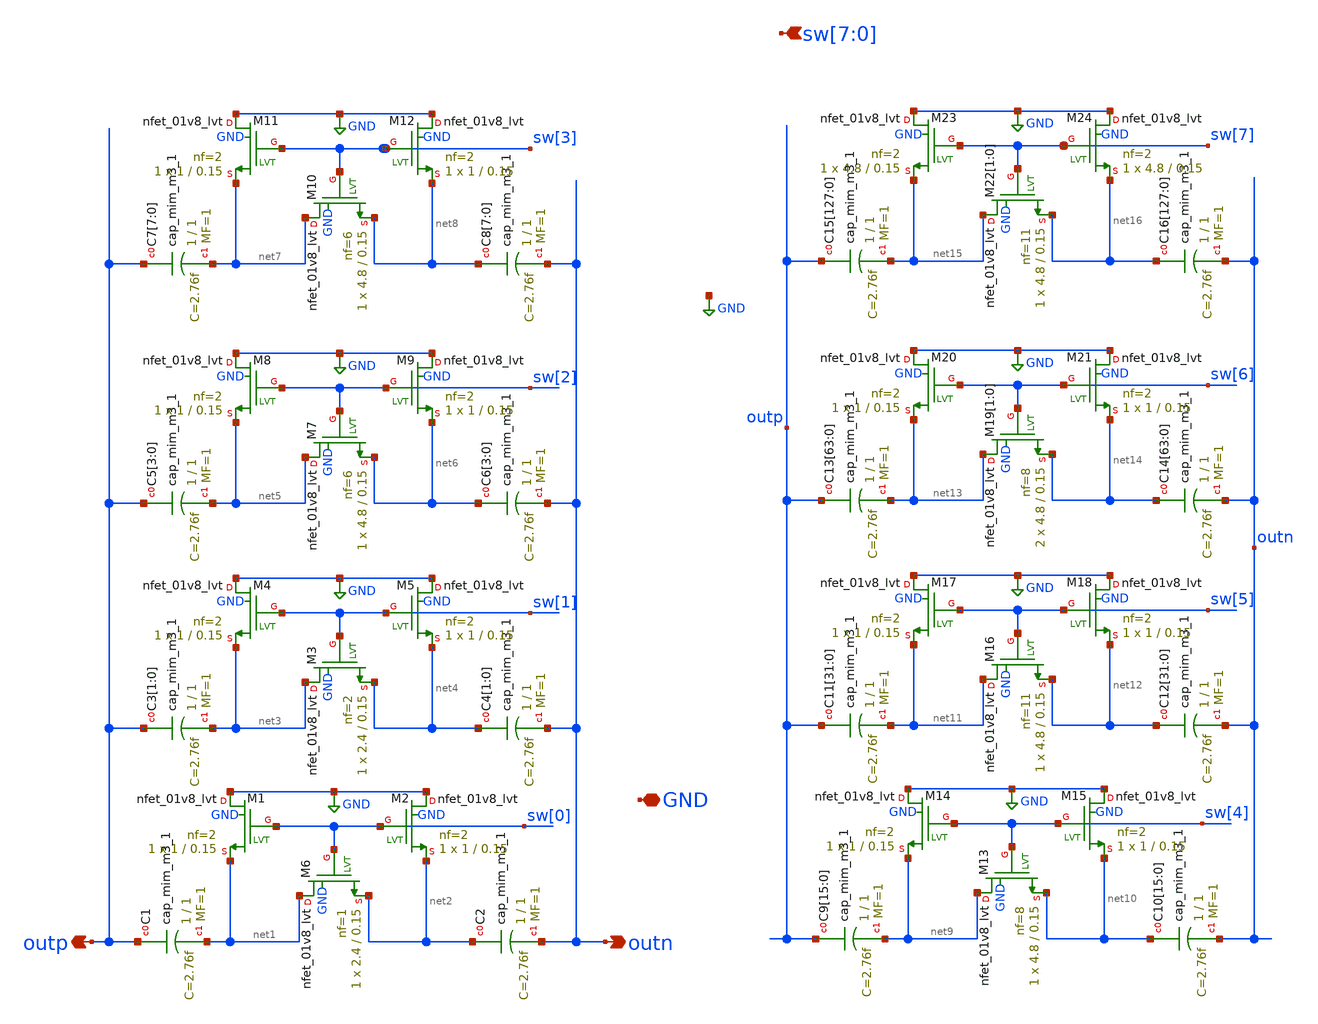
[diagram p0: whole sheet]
** sch_path: openfasoc/generators/lc-dco/xschem_rundir/swcap_3M2C.sch
**.subckt swcap_3M2C outn outp sw[7],sw[6],sw[5],sw[4],sw[3],sw[2],sw[1],sw[0] GND
*.opin outn
*.opin outp
*.ipin sw[7],sw[6],sw[5],sw[4],sw[3],sw[2],sw[1],sw[0]
*.iopin GND
XC2 net2 outn sky130_fd_pr__cap_mim_m3_1 W=1 L=1 MF=1 m=1
XM6 net1 sw[0] net2 GND sky130_fd_pr__nfet_01v8_lvt L=0.15 W=2.4 nf=1 ad='int((nf+1)/2) * W/nf * 0.29'
+ as='int((nf+2)/2) * W/nf * 0.29' pd='2*int((nf+1)/2) * (W/nf + 0.29)' ps='2*int((nf+2)/2) * (W/nf + 0.29)'
+ nrd='0.29 / W' nrs='0.29 / W' sa=0 sb=0 sd=0 mult=1 m=1
XM1 GND sw[0] net1 GND sky130_fd_pr__nfet_01v8_lvt L=0.15 W=1 nf=2 ad='int((nf+1)/2) * W/nf * 0.29' as='int((nf+2)/2) * W/nf * 0.29'
+ pd='2*int((nf+1)/2) * (W/nf + 0.29)' ps='2*int((nf+2)/2) * (W/nf + 0.29)' nrd='0.29 / W' nrs='0.29 / W'
+ sa=0 sb=0 sd=0 mult=1 m=1
XM2 GND sw[0] net2 GND sky130_fd_pr__nfet_01v8_lvt L=0.15 W=1 nf=2 ad='int((nf+1)/2) * W/nf * 0.29' as='int((nf+2)/2) * W/nf * 0.29'
+ pd='2*int((nf+1)/2) * (W/nf + 0.29)' ps='2*int((nf+2)/2) * (W/nf + 0.29)' nrd='0.29 / W' nrs='0.29 / W'
+ sa=0 sb=0 sd=0 mult=1 m=1
XC1 outp net1 sky130_fd_pr__cap_mim_m3_1 W=1 L=1 MF=1 m=1
XC4[1] net4 outn sky130_fd_pr__cap_mim_m3_1 W=1 L=1 MF=1 m=1
XC4[0] net4 outn sky130_fd_pr__cap_mim_m3_1 W=1 L=1 MF=1 m=1
XM3 net3 sw[1] net4 GND sky130_fd_pr__nfet_01v8_lvt L=0.15 W=2.4 nf=2 ad='int((nf+1)/2) * W/nf * 0.29'
+ as='int((nf+2)/2) * W/nf * 0.29' pd='2*int((nf+1)/2) * (W/nf + 0.29)' ps='2*int((nf+2)/2) * (W/nf + 0.29)'
+ nrd='0.29 / W' nrs='0.29 / W' sa=0 sb=0 sd=0 mult=1 m=1
XM4 GND sw[1] net3 GND sky130_fd_pr__nfet_01v8_lvt L=0.15 W=1 nf=2 ad='int((nf+1)/2) * W/nf * 0.29' as='int((nf+2)/2) * W/nf * 0.29'
+ pd='2*int((nf+1)/2) * (W/nf + 0.29)' ps='2*int((nf+2)/2) * (W/nf + 0.29)' nrd='0.29 / W' nrs='0.29 / W'
+ sa=0 sb=0 sd=0 mult=1 m=1
XM5 GND sw[1] net4 GND sky130_fd_pr__nfet_01v8_lvt L=0.15 W=1 nf=2 ad='int((nf+1)/2) * W/nf * 0.29' as='int((nf+2)/2) * W/nf * 0.29'
+ pd='2*int((nf+1)/2) * (W/nf + 0.29)' ps='2*int((nf+2)/2) * (W/nf + 0.29)' nrd='0.29 / W' nrs='0.29 / W'
+ sa=0 sb=0 sd=0 mult=1 m=1
XC3[1] outp net3 sky130_fd_pr__cap_mim_m3_1 W=1 L=1 MF=1 m=1
XC3[0] outp net3 sky130_fd_pr__cap_mim_m3_1 W=1 L=1 MF=1 m=1
XC6[3] net6 outn sky130_fd_pr__cap_mim_m3_1 W=1 L=1 MF=1 m=1
XC6[2] net6 outn sky130_fd_pr__cap_mim_m3_1 W=1 L=1 MF=1 m=1
XC6[1] net6 outn sky130_fd_pr__cap_mim_m3_1 W=1 L=1 MF=1 m=1
XC6[0] net6 outn sky130_fd_pr__cap_mim_m3_1 W=1 L=1 MF=1 m=1
XM7 net5 sw[2] net6 GND sky130_fd_pr__nfet_01v8_lvt L=0.15 W=4.8 nf=6 ad='int((nf+1)/2) * W/nf * 0.29'
+ as='int((nf+2)/2) * W/nf * 0.29' pd='2*int((nf+1)/2) * (W/nf + 0.29)' ps='2*int((nf+2)/2) * (W/nf + 0.29)'
+ nrd='0.29 / W' nrs='0.29 / W' sa=0 sb=0 sd=0 mult=1 m=1
XM8 GND sw[2] net5 GND sky130_fd_pr__nfet_01v8_lvt L=0.15 W=1 nf=2 ad='int((nf+1)/2) * W/nf * 0.29' as='int((nf+2)/2) * W/nf * 0.29'
+ pd='2*int((nf+1)/2) * (W/nf + 0.29)' ps='2*int((nf+2)/2) * (W/nf + 0.29)' nrd='0.29 / W' nrs='0.29 / W'
+ sa=0 sb=0 sd=0 mult=1 m=1
XM9 GND sw[2] net6 GND sky130_fd_pr__nfet_01v8_lvt L=0.15 W=1 nf=2 ad='int((nf+1)/2) * W/nf * 0.29' as='int((nf+2)/2) * W/nf * 0.29'
+ pd='2*int((nf+1)/2) * (W/nf + 0.29)' ps='2*int((nf+2)/2) * (W/nf + 0.29)' nrd='0.29 / W' nrs='0.29 / W'
+ sa=0 sb=0 sd=0 mult=1 m=1
XC5[3] outp net5 sky130_fd_pr__cap_mim_m3_1 W=1 L=1 MF=1 m=1
XC5[2] outp net5 sky130_fd_pr__cap_mim_m3_1 W=1 L=1 MF=1 m=1
XC5[1] outp net5 sky130_fd_pr__cap_mim_m3_1 W=1 L=1 MF=1 m=1
XC5[0] outp net5 sky130_fd_pr__cap_mim_m3_1 W=1 L=1 MF=1 m=1
XC8[7] net8 outn sky130_fd_pr__cap_mim_m3_1 W=1 L=1 MF=1 m=1
XC8[6] net8 outn sky130_fd_pr__cap_mim_m3_1 W=1 L=1 MF=1 m=1
XC8[5] net8 outn sky130_fd_pr__cap_mim_m3_1 W=1 L=1 MF=1 m=1
XC8[4] net8 outn sky130_fd_pr__cap_mim_m3_1 W=1 L=1 MF=1 m=1
XC8[3] net8 outn sky130_fd_pr__cap_mim_m3_1 W=1 L=1 MF=1 m=1
XC8[2] net8 outn sky130_fd_pr__cap_mim_m3_1 W=1 L=1 MF=1 m=1
XC8[1] net8 outn sky130_fd_pr__cap_mim_m3_1 W=1 L=1 MF=1 m=1
XC8[0] net8 outn sky130_fd_pr__cap_mim_m3_1 W=1 L=1 MF=1 m=1
XM10 net7 sw[3] net8 GND sky130_fd_pr__nfet_01v8_lvt L=0.15 W=4.8 nf=6 ad='int((nf+1)/2) * W/nf * 0.29'
+ as='int((nf+2)/2) * W/nf * 0.29' pd='2*int((nf+1)/2) * (W/nf + 0.29)' ps='2*int((nf+2)/2) * (W/nf + 0.29)'
+ nrd='0.29 / W' nrs='0.29 / W' sa=0 sb=0 sd=0 mult=1 m=1
XM11 GND sw[3] net7 GND sky130_fd_pr__nfet_01v8_lvt L=0.15 W=1 nf=2 ad='int((nf+1)/2) * W/nf * 0.29'
+ as='int((nf+2)/2) * W/nf * 0.29' pd='2*int((nf+1)/2) * (W/nf + 0.29)' ps='2*int((nf+2)/2) * (W/nf + 0.29)'
+ nrd='0.29 / W' nrs='0.29 / W' sa=0 sb=0 sd=0 mult=1 m=1
XM12 GND sw[3] net8 GND sky130_fd_pr__nfet_01v8_lvt L=0.15 W=1 nf=2 ad='int((nf+1)/2) * W/nf * 0.29'
+ as='int((nf+2)/2) * W/nf * 0.29' pd='2*int((nf+1)/2) * (W/nf + 0.29)' ps='2*int((nf+2)/2) * (W/nf + 0.29)'
+ nrd='0.29 / W' nrs='0.29 / W' sa=0 sb=0 sd=0 mult=1 m=1
XC7[7] outp net7 sky130_fd_pr__cap_mim_m3_1 W=1 L=1 MF=1 m=1
XC7[6] outp net7 sky130_fd_pr__cap_mim_m3_1 W=1 L=1 MF=1 m=1
XC7[5] outp net7 sky130_fd_pr__cap_mim_m3_1 W=1 L=1 MF=1 m=1
XC7[4] outp net7 sky130_fd_pr__cap_mim_m3_1 W=1 L=1 MF=1 m=1
XC7[3] outp net7 sky130_fd_pr__cap_mim_m3_1 W=1 L=1 MF=1 m=1
XC7[2] outp net7 sky130_fd_pr__cap_mim_m3_1 W=1 L=1 MF=1 m=1
XC7[1] outp net7 sky130_fd_pr__cap_mim_m3_1 W=1 L=1 MF=1 m=1
XC7[0] outp net7 sky130_fd_pr__cap_mim_m3_1 W=1 L=1 MF=1 m=1
XC10[15] net10 outn sky130_fd_pr__cap_mim_m3_1 W=1 L=1 MF=1 m=1
XC10[14] net10 outn sky130_fd_pr__cap_mim_m3_1 W=1 L=1 MF=1 m=1
XC10[13] net10 outn sky130_fd_pr__cap_mim_m3_1 W=1 L=1 MF=1 m=1
XC10[12] net10 outn sky130_fd_pr__cap_mim_m3_1 W=1 L=1 MF=1 m=1
XC10[11] net10 outn sky130_fd_pr__cap_mim_m3_1 W=1 L=1 MF=1 m=1
XC10[10] net10 outn sky130_fd_pr__cap_mim_m3_1 W=1 L=1 MF=1 m=1
XC10[9] net10 outn sky130_fd_pr__cap_mim_m3_1 W=1 L=1 MF=1 m=1
XC10[8] net10 outn sky130_fd_pr__cap_mim_m3_1 W=1 L=1 MF=1 m=1
XC10[7] net10 outn sky130_fd_pr__cap_mim_m3_1 W=1 L=1 MF=1 m=1
XC10[6] net10 outn sky130_fd_pr__cap_mim_m3_1 W=1 L=1 MF=1 m=1
XC10[5] net10 outn sky130_fd_pr__cap_mim_m3_1 W=1 L=1 MF=1 m=1
XC10[4] net10 outn sky130_fd_pr__cap_mim_m3_1 W=1 L=1 MF=1 m=1
XC10[3] net10 outn sky130_fd_pr__cap_mim_m3_1 W=1 L=1 MF=1 m=1
XC10[2] net10 outn sky130_fd_pr__cap_mim_m3_1 W=1 L=1 MF=1 m=1
XC10[1] net10 outn sky130_fd_pr__cap_mim_m3_1 W=1 L=1 MF=1 m=1
XC10[0] net10 outn sky130_fd_pr__cap_mim_m3_1 W=1 L=1 MF=1 m=1
XM13 net9 sw[4] net10 GND sky130_fd_pr__nfet_01v8_lvt L=0.15 W=4.8 nf=8 ad='int((nf+1)/2) * W/nf * 0.29'
+ as='int((nf+2)/2) * W/nf * 0.29' pd='2*int((nf+1)/2) * (W/nf + 0.29)' ps='2*int((nf+2)/2) * (W/nf + 0.29)'
+ nrd='0.29 / W' nrs='0.29 / W' sa=0 sb=0 sd=0 mult=1 m=1
XM14 GND sw[4] net9 GND sky130_fd_pr__nfet_01v8_lvt L=0.15 W=1 nf=2 ad='int((nf+1)/2) * W/nf * 0.29'
+ as='int((nf+2)/2) * W/nf * 0.29' pd='2*int((nf+1)/2) * (W/nf + 0.29)' ps='2*int((nf+2)/2) * (W/nf + 0.29)'
+ nrd='0.29 / W' nrs='0.29 / W' sa=0 sb=0 sd=0 mult=1 m=1
XM15 GND sw[4] net10 GND sky130_fd_pr__nfet_01v8_lvt L=0.15 W=1 nf=2 ad='int((nf+1)/2) * W/nf * 0.29'
+ as='int((nf+2)/2) * W/nf * 0.29' pd='2*int((nf+1)/2) * (W/nf + 0.29)' ps='2*int((nf+2)/2) * (W/nf + 0.29)'
+ nrd='0.29 / W' nrs='0.29 / W' sa=0 sb=0 sd=0 mult=1 m=1
XC9[15] outp net9 sky130_fd_pr__cap_mim_m3_1 W=1 L=1 MF=1 m=1
XC9[14] outp net9 sky130_fd_pr__cap_mim_m3_1 W=1 L=1 MF=1 m=1
XC9[13] outp net9 sky130_fd_pr__cap_mim_m3_1 W=1 L=1 MF=1 m=1
XC9[12] outp net9 sky130_fd_pr__cap_mim_m3_1 W=1 L=1 MF=1 m=1
XC9[11] outp net9 sky130_fd_pr__cap_mim_m3_1 W=1 L=1 MF=1 m=1
XC9[10] outp net9 sky130_fd_pr__cap_mim_m3_1 W=1 L=1 MF=1 m=1
XC9[9] outp net9 sky130_fd_pr__cap_mim_m3_1 W=1 L=1 MF=1 m=1
XC9[8] outp net9 sky130_fd_pr__cap_mim_m3_1 W=1 L=1 MF=1 m=1
XC9[7] outp net9 sky130_fd_pr__cap_mim_m3_1 W=1 L=1 MF=1 m=1
XC9[6] outp net9 sky130_fd_pr__cap_mim_m3_1 W=1 L=1 MF=1 m=1
XC9[5] outp net9 sky130_fd_pr__cap_mim_m3_1 W=1 L=1 MF=1 m=1
XC9[4] outp net9 sky130_fd_pr__cap_mim_m3_1 W=1 L=1 MF=1 m=1
XC9[3] outp net9 sky130_fd_pr__cap_mim_m3_1 W=1 L=1 MF=1 m=1
XC9[2] outp net9 sky130_fd_pr__cap_mim_m3_1 W=1 L=1 MF=1 m=1
XC9[1] outp net9 sky130_fd_pr__cap_mim_m3_1 W=1 L=1 MF=1 m=1
XC9[0] outp net9 sky130_fd_pr__cap_mim_m3_1 W=1 L=1 MF=1 m=1
XC12[31] net12 outn sky130_fd_pr__cap_mim_m3_1 W=1 L=1 MF=1 m=1
XC12[30] net12 outn sky130_fd_pr__cap_mim_m3_1 W=1 L=1 MF=1 m=1
XC12[29] net12 outn sky130_fd_pr__cap_mim_m3_1 W=1 L=1 MF=1 m=1
XC12[28] net12 outn sky130_fd_pr__cap_mim_m3_1 W=1 L=1 MF=1 m=1
XC12[27] net12 outn sky130_fd_pr__cap_mim_m3_1 W=1 L=1 MF=1 m=1
XC12[26] net12 outn sky130_fd_pr__cap_mim_m3_1 W=1 L=1 MF=1 m=1
XC12[25] net12 outn sky130_fd_pr__cap_mim_m3_1 W=1 L=1 MF=1 m=1
XC12[24] net12 outn sky130_fd_pr__cap_mim_m3_1 W=1 L=1 MF=1 m=1
XC12[23] net12 outn sky130_fd_pr__cap_mim_m3_1 W=1 L=1 MF=1 m=1
XC12[22] net12 outn sky130_fd_pr__cap_mim_m3_1 W=1 L=1 MF=1 m=1
XC12[21] net12 outn sky130_fd_pr__cap_mim_m3_1 W=1 L=1 MF=1 m=1
XC12[20] net12 outn sky130_fd_pr__cap_mim_m3_1 W=1 L=1 MF=1 m=1
XC12[19] net12 outn sky130_fd_pr__cap_mim_m3_1 W=1 L=1 MF=1 m=1
XC12[18] net12 outn sky130_fd_pr__cap_mim_m3_1 W=1 L=1 MF=1 m=1
XC12[17] net12 outn sky130_fd_pr__cap_mim_m3_1 W=1 L=1 MF=1 m=1
XC12[16] net12 outn sky130_fd_pr__cap_mim_m3_1 W=1 L=1 MF=1 m=1
XC12[15] net12 outn sky130_fd_pr__cap_mim_m3_1 W=1 L=1 MF=1 m=1
XC12[14] net12 outn sky130_fd_pr__cap_mim_m3_1 W=1 L=1 MF=1 m=1
XC12[13] net12 outn sky130_fd_pr__cap_mim_m3_1 W=1 L=1 MF=1 m=1
XC12[12] net12 outn sky130_fd_pr__cap_mim_m3_1 W=1 L=1 MF=1 m=1
XC12[11] net12 outn sky130_fd_pr__cap_mim_m3_1 W=1 L=1 MF=1 m=1
XC12[10] net12 outn sky130_fd_pr__cap_mim_m3_1 W=1 L=1 MF=1 m=1
XC12[9] net12 outn sky130_fd_pr__cap_mim_m3_1 W=1 L=1 MF=1 m=1
XC12[8] net12 outn sky130_fd_pr__cap_mim_m3_1 W=1 L=1 MF=1 m=1
XC12[7] net12 outn sky130_fd_pr__cap_mim_m3_1 W=1 L=1 MF=1 m=1
XC12[6] net12 outn sky130_fd_pr__cap_mim_m3_1 W=1 L=1 MF=1 m=1
XC12[5] net12 outn sky130_fd_pr__cap_mim_m3_1 W=1 L=1 MF=1 m=1
XC12[4] net12 outn sky130_fd_pr__cap_mim_m3_1 W=1 L=1 MF=1 m=1
XC12[3] net12 outn sky130_fd_pr__cap_mim_m3_1 W=1 L=1 MF=1 m=1
XC12[2] net12 outn sky130_fd_pr__cap_mim_m3_1 W=1 L=1 MF=1 m=1
XC12[1] net12 outn sky130_fd_pr__cap_mim_m3_1 W=1 L=1 MF=1 m=1
XC12[0] net12 outn sky130_fd_pr__cap_mim_m3_1 W=1 L=1 MF=1 m=1
XM16 net11 sw[5] net12 GND sky130_fd_pr__nfet_01v8_lvt L=0.15 W=4.8 nf=11 ad='int((nf+1)/2) * W/nf * 0.29'
+ as='int((nf+2)/2) * W/nf * 0.29' pd='2*int((nf+1)/2) * (W/nf + 0.29)' ps='2*int((nf+2)/2) * (W/nf + 0.29)'
+ nrd='0.29 / W' nrs='0.29 / W' sa=0 sb=0 sd=0 mult=1 m=1
XM17 GND sw[5] net11 GND sky130_fd_pr__nfet_01v8_lvt L=0.15 W=1 nf=2 ad='int((nf+1)/2) * W/nf * 0.29'
+ as='int((nf+2)/2) * W/nf * 0.29' pd='2*int((nf+1)/2) * (W/nf + 0.29)' ps='2*int((nf+2)/2) * (W/nf + 0.29)'
+ nrd='0.29 / W' nrs='0.29 / W' sa=0 sb=0 sd=0 mult=1 m=1
XM18 GND sw[5] net12 GND sky130_fd_pr__nfet_01v8_lvt L=0.15 W=1 nf=2 ad='int((nf+1)/2) * W/nf * 0.29'
+ as='int((nf+2)/2) * W/nf * 0.29' pd='2*int((nf+1)/2) * (W/nf + 0.29)' ps='2*int((nf+2)/2) * (W/nf + 0.29)'
+ nrd='0.29 / W' nrs='0.29 / W' sa=0 sb=0 sd=0 mult=1 m=1
XC11[31] outp net11 sky130_fd_pr__cap_mim_m3_1 W=1 L=1 MF=1 m=1
XC11[30] outp net11 sky130_fd_pr__cap_mim_m3_1 W=1 L=1 MF=1 m=1
XC11[29] outp net11 sky130_fd_pr__cap_mim_m3_1 W=1 L=1 MF=1 m=1
XC11[28] outp net11 sky130_fd_pr__cap_mim_m3_1 W=1 L=1 MF=1 m=1
XC11[27] outp net11 sky130_fd_pr__cap_mim_m3_1 W=1 L=1 MF=1 m=1
XC11[26] outp net11 sky130_fd_pr__cap_mim_m3_1 W=1 L=1 MF=1 m=1
XC11[25] outp net11 sky130_fd_pr__cap_mim_m3_1 W=1 L=1 MF=1 m=1
XC11[24] outp net11 sky130_fd_pr__cap_mim_m3_1 W=1 L=1 MF=1 m=1
XC11[23] outp net11 sky130_fd_pr__cap_mim_m3_1 W=1 L=1 MF=1 m=1
XC11[22] outp net11 sky130_fd_pr__cap_mim_m3_1 W=1 L=1 MF=1 m=1
XC11[21] outp net11 sky130_fd_pr__cap_mim_m3_1 W=1 L=1 MF=1 m=1
XC11[20] outp net11 sky130_fd_pr__cap_mim_m3_1 W=1 L=1 MF=1 m=1
XC11[19] outp net11 sky130_fd_pr__cap_mim_m3_1 W=1 L=1 MF=1 m=1
XC11[18] outp net11 sky130_fd_pr__cap_mim_m3_1 W=1 L=1 MF=1 m=1
XC11[17] outp net11 sky130_fd_pr__cap_mim_m3_1 W=1 L=1 MF=1 m=1
XC11[16] outp net11 sky130_fd_pr__cap_mim_m3_1 W=1 L=1 MF=1 m=1
XC11[15] outp net11 sky130_fd_pr__cap_mim_m3_1 W=1 L=1 MF=1 m=1
XC11[14] outp net11 sky130_fd_pr__cap_mim_m3_1 W=1 L=1 MF=1 m=1
XC11[13] outp net11 sky130_fd_pr__cap_mim_m3_1 W=1 L=1 MF=1 m=1
XC11[12] outp net11 sky130_fd_pr__cap_mim_m3_1 W=1 L=1 MF=1 m=1
XC11[11] outp net11 sky130_fd_pr__cap_mim_m3_1 W=1 L=1 MF=1 m=1
XC11[10] outp net11 sky130_fd_pr__cap_mim_m3_1 W=1 L=1 MF=1 m=1
XC11[9] outp net11 sky130_fd_pr__cap_mim_m3_1 W=1 L=1 MF=1 m=1
XC11[8] outp net11 sky130_fd_pr__cap_mim_m3_1 W=1 L=1 MF=1 m=1
XC11[7] outp net11 sky130_fd_pr__cap_mim_m3_1 W=1 L=1 MF=1 m=1
XC11[6] outp net11 sky130_fd_pr__cap_mim_m3_1 W=1 L=1 MF=1 m=1
XC11[5] outp net11 sky130_fd_pr__cap_mim_m3_1 W=1 L=1 MF=1 m=1
XC11[4] outp net11 sky130_fd_pr__cap_mim_m3_1 W=1 L=1 MF=1 m=1
XC11[3] outp net11 sky130_fd_pr__cap_mim_m3_1 W=1 L=1 MF=1 m=1
XC11[2] outp net11 sky130_fd_pr__cap_mim_m3_1 W=1 L=1 MF=1 m=1
XC11[1] outp net11 sky130_fd_pr__cap_mim_m3_1 W=1 L=1 MF=1 m=1
XC11[0] outp net11 sky130_fd_pr__cap_mim_m3_1 W=1 L=1 MF=1 m=1
XC14[63] net14 outn sky130_fd_pr__cap_mim_m3_1 W=1 L=1 MF=1 m=1
XC14[62] net14 outn sky130_fd_pr__cap_mim_m3_1 W=1 L=1 MF=1 m=1
XC14[61] net14 outn sky130_fd_pr__cap_mim_m3_1 W=1 L=1 MF=1 m=1
XC14[60] net14 outn sky130_fd_pr__cap_mim_m3_1 W=1 L=1 MF=1 m=1
XC14[59] net14 outn sky130_fd_pr__cap_mim_m3_1 W=1 L=1 MF=1 m=1
XC14[58] net14 outn sky130_fd_pr__cap_mim_m3_1 W=1 L=1 MF=1 m=1
XC14[57] net14 outn sky130_fd_pr__cap_mim_m3_1 W=1 L=1 MF=1 m=1
XC14[56] net14 outn sky130_fd_pr__cap_mim_m3_1 W=1 L=1 MF=1 m=1
XC14[55] net14 outn sky130_fd_pr__cap_mim_m3_1 W=1 L=1 MF=1 m=1
XC14[54] net14 outn sky130_fd_pr__cap_mim_m3_1 W=1 L=1 MF=1 m=1
XC14[53] net14 outn sky130_fd_pr__cap_mim_m3_1 W=1 L=1 MF=1 m=1
XC14[52] net14 outn sky130_fd_pr__cap_mim_m3_1 W=1 L=1 MF=1 m=1
XC14[51] net14 outn sky130_fd_pr__cap_mim_m3_1 W=1 L=1 MF=1 m=1
XC14[50] net14 outn sky130_fd_pr__cap_mim_m3_1 W=1 L=1 MF=1 m=1
XC14[49] net14 outn sky130_fd_pr__cap_mim_m3_1 W=1 L=1 MF=1 m=1
XC14[48] net14 outn sky130_fd_pr__cap_mim_m3_1 W=1 L=1 MF=1 m=1
XC14[47] net14 outn sky130_fd_pr__cap_mim_m3_1 W=1 L=1 MF=1 m=1
XC14[46] net14 outn sky130_fd_pr__cap_mim_m3_1 W=1 L=1 MF=1 m=1
XC14[45] net14 outn sky130_fd_pr__cap_mim_m3_1 W=1 L=1 MF=1 m=1
XC14[44] net14 outn sky130_fd_pr__cap_mim_m3_1 W=1 L=1 MF=1 m=1
XC14[43] net14 outn sky130_fd_pr__cap_mim_m3_1 W=1 L=1 MF=1 m=1
XC14[42] net14 outn sky130_fd_pr__cap_mim_m3_1 W=1 L=1 MF=1 m=1
XC14[41] net14 outn sky130_fd_pr__cap_mim_m3_1 W=1 L=1 MF=1 m=1
XC14[40] net14 outn sky130_fd_pr__cap_mim_m3_1 W=1 L=1 MF=1 m=1
XC14[39] net14 outn sky130_fd_pr__cap_mim_m3_1 W=1 L=1 MF=1 m=1
XC14[38] net14 outn sky130_fd_pr__cap_mim_m3_1 W=1 L=1 MF=1 m=1
XC14[37] net14 outn sky130_fd_pr__cap_mim_m3_1 W=1 L=1 MF=1 m=1
XC14[36] net14 outn sky130_fd_pr__cap_mim_m3_1 W=1 L=1 MF=1 m=1
XC14[35] net14 outn sky130_fd_pr__cap_mim_m3_1 W=1 L=1 MF=1 m=1
XC14[34] net14 outn sky130_fd_pr__cap_mim_m3_1 W=1 L=1 MF=1 m=1
XC14[33] net14 outn sky130_fd_pr__cap_mim_m3_1 W=1 L=1 MF=1 m=1
XC14[32] net14 outn sky130_fd_pr__cap_mim_m3_1 W=1 L=1 MF=1 m=1
XC14[31] net14 outn sky130_fd_pr__cap_mim_m3_1 W=1 L=1 MF=1 m=1
XC14[30] net14 outn sky130_fd_pr__cap_mim_m3_1 W=1 L=1 MF=1 m=1
XC14[29] net14 outn sky130_fd_pr__cap_mim_m3_1 W=1 L=1 MF=1 m=1
XC14[28] net14 outn sky130_fd_pr__cap_mim_m3_1 W=1 L=1 MF=1 m=1
XC14[27] net14 outn sky130_fd_pr__cap_mim_m3_1 W=1 L=1 MF=1 m=1
XC14[26] net14 outn sky130_fd_pr__cap_mim_m3_1 W=1 L=1 MF=1 m=1
XC14[25] net14 outn sky130_fd_pr__cap_mim_m3_1 W=1 L=1 MF=1 m=1
XC14[24] net14 outn sky130_fd_pr__cap_mim_m3_1 W=1 L=1 MF=1 m=1
XC14[23] net14 outn sky130_fd_pr__cap_mim_m3_1 W=1 L=1 MF=1 m=1
XC14[22] net14 outn sky130_fd_pr__cap_mim_m3_1 W=1 L=1 MF=1 m=1
XC14[21] net14 outn sky130_fd_pr__cap_mim_m3_1 W=1 L=1 MF=1 m=1
XC14[20] net14 outn sky130_fd_pr__cap_mim_m3_1 W=1 L=1 MF=1 m=1
XC14[19] net14 outn sky130_fd_pr__cap_mim_m3_1 W=1 L=1 MF=1 m=1
XC14[18] net14 outn sky130_fd_pr__cap_mim_m3_1 W=1 L=1 MF=1 m=1
XC14[17] net14 outn sky130_fd_pr__cap_mim_m3_1 W=1 L=1 MF=1 m=1
XC14[16] net14 outn sky130_fd_pr__cap_mim_m3_1 W=1 L=1 MF=1 m=1
XC14[15] net14 outn sky130_fd_pr__cap_mim_m3_1 W=1 L=1 MF=1 m=1
XC14[14] net14 outn sky130_fd_pr__cap_mim_m3_1 W=1 L=1 MF=1 m=1
XC14[13] net14 outn sky130_fd_pr__cap_mim_m3_1 W=1 L=1 MF=1 m=1
XC14[12] net14 outn sky130_fd_pr__cap_mim_m3_1 W=1 L=1 MF=1 m=1
XC14[11] net14 outn sky130_fd_pr__cap_mim_m3_1 W=1 L=1 MF=1 m=1
XC14[10] net14 outn sky130_fd_pr__cap_mim_m3_1 W=1 L=1 MF=1 m=1
XC14[9] net14 outn sky130_fd_pr__cap_mim_m3_1 W=1 L=1 MF=1 m=1
XC14[8] net14 outn sky130_fd_pr__cap_mim_m3_1 W=1 L=1 MF=1 m=1
XC14[7] net14 outn sky130_fd_pr__cap_mim_m3_1 W=1 L=1 MF=1 m=1
XC14[6] net14 outn sky130_fd_pr__cap_mim_m3_1 W=1 L=1 MF=1 m=1
XC14[5] net14 outn sky130_fd_pr__cap_mim_m3_1 W=1 L=1 MF=1 m=1
XC14[4] net14 outn sky130_fd_pr__cap_mim_m3_1 W=1 L=1 MF=1 m=1
XC14[3] net14 outn sky130_fd_pr__cap_mim_m3_1 W=1 L=1 MF=1 m=1
XC14[2] net14 outn sky130_fd_pr__cap_mim_m3_1 W=1 L=1 MF=1 m=1
XC14[1] net14 outn sky130_fd_pr__cap_mim_m3_1 W=1 L=1 MF=1 m=1
XC14[0] net14 outn sky130_fd_pr__cap_mim_m3_1 W=1 L=1 MF=1 m=1
XM19[1] net13 sw[6] net14 GND sky130_fd_pr__nfet_01v8_lvt L=0.15 W=4.8 nf=8 ad='int((nf+1)/2) * W/nf * 0.29'
+ as='int((nf+2)/2) * W/nf * 0.29' pd='2*int((nf+1)/2) * (W/nf + 0.29)' ps='2*int((nf+2)/2) * (W/nf + 0.29)'
+ nrd='0.29 / W' nrs='0.29 / W' sa=0 sb=0 sd=0 mult=2 m=2
XM19[0] net13 sw[6] net14 GND sky130_fd_pr__nfet_01v8_lvt L=0.15 W=4.8 nf=8 ad='int((nf+1)/2) * W/nf * 0.29'
+ as='int((nf+2)/2) * W/nf * 0.29' pd='2*int((nf+1)/2) * (W/nf + 0.29)' ps='2*int((nf+2)/2) * (W/nf + 0.29)'
+ nrd='0.29 / W' nrs='0.29 / W' sa=0 sb=0 sd=0 mult=2 m=2
XM20 GND sw[6] net13 GND sky130_fd_pr__nfet_01v8_lvt L=0.15 W=1 nf=2 ad='int((nf+1)/2) * W/nf * 0.29'
+ as='int((nf+2)/2) * W/nf * 0.29' pd='2*int((nf+1)/2) * (W/nf + 0.29)' ps='2*int((nf+2)/2) * (W/nf + 0.29)'
+ nrd='0.29 / W' nrs='0.29 / W' sa=0 sb=0 sd=0 mult=1 m=1
XM21 GND sw[6] net14 GND sky130_fd_pr__nfet_01v8_lvt L=0.15 W=1 nf=2 ad='int((nf+1)/2) * W/nf * 0.29'
+ as='int((nf+2)/2) * W/nf * 0.29' pd='2*int((nf+1)/2) * (W/nf + 0.29)' ps='2*int((nf+2)/2) * (W/nf + 0.29)'
+ nrd='0.29 / W' nrs='0.29 / W' sa=0 sb=0 sd=0 mult=1 m=1
XC13[63] outp net13 sky130_fd_pr__cap_mim_m3_1 W=1 L=1 MF=1 m=1
XC13[62] outp net13 sky130_fd_pr__cap_mim_m3_1 W=1 L=1 MF=1 m=1
XC13[61] outp net13 sky130_fd_pr__cap_mim_m3_1 W=1 L=1 MF=1 m=1
XC13[60] outp net13 sky130_fd_pr__cap_mim_m3_1 W=1 L=1 MF=1 m=1
XC13[59] outp net13 sky130_fd_pr__cap_mim_m3_1 W=1 L=1 MF=1 m=1
XC13[58] outp net13 sky130_fd_pr__cap_mim_m3_1 W=1 L=1 MF=1 m=1
XC13[57] outp net13 sky130_fd_pr__cap_mim_m3_1 W=1 L=1 MF=1 m=1
XC13[56] outp net13 sky130_fd_pr__cap_mim_m3_1 W=1 L=1 MF=1 m=1
XC13[55] outp net13 sky130_fd_pr__cap_mim_m3_1 W=1 L=1 MF=1 m=1
XC13[54] outp net13 sky130_fd_pr__cap_mim_m3_1 W=1 L=1 MF=1 m=1
XC13[53] outp net13 sky130_fd_pr__cap_mim_m3_1 W=1 L=1 MF=1 m=1
XC13[52] outp net13 sky130_fd_pr__cap_mim_m3_1 W=1 L=1 MF=1 m=1
XC13[51] outp net13 sky130_fd_pr__cap_mim_m3_1 W=1 L=1 MF=1 m=1
XC13[50] outp net13 sky130_fd_pr__cap_mim_m3_1 W=1 L=1 MF=1 m=1
XC13[49] outp net13 sky130_fd_pr__cap_mim_m3_1 W=1 L=1 MF=1 m=1
XC13[48] outp net13 sky130_fd_pr__cap_mim_m3_1 W=1 L=1 MF=1 m=1
XC13[47] outp net13 sky130_fd_pr__cap_mim_m3_1 W=1 L=1 MF=1 m=1
XC13[46] outp net13 sky130_fd_pr__cap_mim_m3_1 W=1 L=1 MF=1 m=1
XC13[45] outp net13 sky130_fd_pr__cap_mim_m3_1 W=1 L=1 MF=1 m=1
XC13[44] outp net13 sky130_fd_pr__cap_mim_m3_1 W=1 L=1 MF=1 m=1
XC13[43] outp net13 sky130_fd_pr__cap_mim_m3_1 W=1 L=1 MF=1 m=1
XC13[42] outp net13 sky130_fd_pr__cap_mim_m3_1 W=1 L=1 MF=1 m=1
XC13[41] outp net13 sky130_fd_pr__cap_mim_m3_1 W=1 L=1 MF=1 m=1
XC13[40] outp net13 sky130_fd_pr__cap_mim_m3_1 W=1 L=1 MF=1 m=1
XC13[39] outp net13 sky130_fd_pr__cap_mim_m3_1 W=1 L=1 MF=1 m=1
XC13[38] outp net13 sky130_fd_pr__cap_mim_m3_1 W=1 L=1 MF=1 m=1
XC13[37] outp net13 sky130_fd_pr__cap_mim_m3_1 W=1 L=1 MF=1 m=1
XC13[36] outp net13 sky130_fd_pr__cap_mim_m3_1 W=1 L=1 MF=1 m=1
XC13[35] outp net13 sky130_fd_pr__cap_mim_m3_1 W=1 L=1 MF=1 m=1
XC13[34] outp net13 sky130_fd_pr__cap_mim_m3_1 W=1 L=1 MF=1 m=1
XC13[33] outp net13 sky130_fd_pr__cap_mim_m3_1 W=1 L=1 MF=1 m=1
XC13[32] outp net13 sky130_fd_pr__cap_mim_m3_1 W=1 L=1 MF=1 m=1
XC13[31] outp net13 sky130_fd_pr__cap_mim_m3_1 W=1 L=1 MF=1 m=1
XC13[30] outp net13 sky130_fd_pr__cap_mim_m3_1 W=1 L=1 MF=1 m=1
XC13[29] outp net13 sky130_fd_pr__cap_mim_m3_1 W=1 L=1 MF=1 m=1
XC13[28] outp net13 sky130_fd_pr__cap_mim_m3_1 W=1 L=1 MF=1 m=1
XC13[27] outp net13 sky130_fd_pr__cap_mim_m3_1 W=1 L=1 MF=1 m=1
XC13[26] outp net13 sky130_fd_pr__cap_mim_m3_1 W=1 L=1 MF=1 m=1
XC13[25] outp net13 sky130_fd_pr__cap_mim_m3_1 W=1 L=1 MF=1 m=1
XC13[24] outp net13 sky130_fd_pr__cap_mim_m3_1 W=1 L=1 MF=1 m=1
XC13[23] outp net13 sky130_fd_pr__cap_mim_m3_1 W=1 L=1 MF=1 m=1
XC13[22] outp net13 sky130_fd_pr__cap_mim_m3_1 W=1 L=1 MF=1 m=1
XC13[21] outp net13 sky130_fd_pr__cap_mim_m3_1 W=1 L=1 MF=1 m=1
XC13[20] outp net13 sky130_fd_pr__cap_mim_m3_1 W=1 L=1 MF=1 m=1
XC13[19] outp net13 sky130_fd_pr__cap_mim_m3_1 W=1 L=1 MF=1 m=1
XC13[18] outp net13 sky130_fd_pr__cap_mim_m3_1 W=1 L=1 MF=1 m=1
XC13[17] outp net13 sky130_fd_pr__cap_mim_m3_1 W=1 L=1 MF=1 m=1
XC13[16] outp net13 sky130_fd_pr__cap_mim_m3_1 W=1 L=1 MF=1 m=1
XC13[15] outp net13 sky130_fd_pr__cap_mim_m3_1 W=1 L=1 MF=1 m=1
XC13[14] outp net13 sky130_fd_pr__cap_mim_m3_1 W=1 L=1 MF=1 m=1
XC13[13] outp net13 sky130_fd_pr__cap_mim_m3_1 W=1 L=1 MF=1 m=1
XC13[12] outp net13 sky130_fd_pr__cap_mim_m3_1 W=1 L=1 MF=1 m=1
XC13[11] outp net13 sky130_fd_pr__cap_mim_m3_1 W=1 L=1 MF=1 m=1
XC13[10] outp net13 sky130_fd_pr__cap_mim_m3_1 W=1 L=1 MF=1 m=1
XC13[9] outp net13 sky130_fd_pr__cap_mim_m3_1 W=1 L=1 MF=1 m=1
XC13[8] outp net13 sky130_fd_pr__cap_mim_m3_1 W=1 L=1 MF=1 m=1
XC13[7] outp net13 sky130_fd_pr__cap_mim_m3_1 W=1 L=1 MF=1 m=1
XC13[6] outp net13 sky130_fd_pr__cap_mim_m3_1 W=1 L=1 MF=1 m=1
XC13[5] outp net13 sky130_fd_pr__cap_mim_m3_1 W=1 L=1 MF=1 m=1
XC13[4] outp net13 sky130_fd_pr__cap_mim_m3_1 W=1 L=1 MF=1 m=1
XC13[3] outp net13 sky130_fd_pr__cap_mim_m3_1 W=1 L=1 MF=1 m=1
XC13[2] outp net13 sky130_fd_pr__cap_mim_m3_1 W=1 L=1 MF=1 m=1
XC13[1] outp net13 sky130_fd_pr__cap_mim_m3_1 W=1 L=1 MF=1 m=1
XC13[0] outp net13 sky130_fd_pr__cap_mim_m3_1 W=1 L=1 MF=1 m=1
XC16[127] net16 outn sky130_fd_pr__cap_mim_m3_1 W=1 L=1 MF=1 m=1
XC16[126] net16 outn sky130_fd_pr__cap_mim_m3_1 W=1 L=1 MF=1 m=1
XC16[125] net16 outn sky130_fd_pr__cap_mim_m3_1 W=1 L=1 MF=1 m=1
XC16[124] net16 outn sky130_fd_pr__cap_mim_m3_1 W=1 L=1 MF=1 m=1
XC16[123] net16 outn sky130_fd_pr__cap_mim_m3_1 W=1 L=1 MF=1 m=1
XC16[122] net16 outn sky130_fd_pr__cap_mim_m3_1 W=1 L=1 MF=1 m=1
XC16[121] net16 outn sky130_fd_pr__cap_mim_m3_1 W=1 L=1 MF=1 m=1
XC16[120] net16 outn sky130_fd_pr__cap_mim_m3_1 W=1 L=1 MF=1 m=1
XC16[119] net16 outn sky130_fd_pr__cap_mim_m3_1 W=1 L=1 MF=1 m=1
XC16[118] net16 outn sky130_fd_pr__cap_mim_m3_1 W=1 L=1 MF=1 m=1
XC16[117] net16 outn sky130_fd_pr__cap_mim_m3_1 W=1 L=1 MF=1 m=1
XC16[116] net16 outn sky130_fd_pr__cap_mim_m3_1 W=1 L=1 MF=1 m=1
XC16[115] net16 outn sky130_fd_pr__cap_mim_m3_1 W=1 L=1 MF=1 m=1
XC16[114] net16 outn sky130_fd_pr__cap_mim_m3_1 W=1 L=1 MF=1 m=1
XC16[113] net16 outn sky130_fd_pr__cap_mim_m3_1 W=1 L=1 MF=1 m=1
XC16[112] net16 outn sky130_fd_pr__cap_mim_m3_1 W=1 L=1 MF=1 m=1
XC16[111] net16 outn sky130_fd_pr__cap_mim_m3_1 W=1 L=1 MF=1 m=1
XC16[110] net16 outn sky130_fd_pr__cap_mim_m3_1 W=1 L=1 MF=1 m=1
XC16[109] net16 outn sky130_fd_pr__cap_mim_m3_1 W=1 L=1 MF=1 m=1
XC16[108] net16 outn sky130_fd_pr__cap_mim_m3_1 W=1 L=1 MF=1 m=1
XC16[107] net16 outn sky130_fd_pr__cap_mim_m3_1 W=1 L=1 MF=1 m=1
XC16[106] net16 outn sky130_fd_pr__cap_mim_m3_1 W=1 L=1 MF=1 m=1
XC16[105] net16 outn sky130_fd_pr__cap_mim_m3_1 W=1 L=1 MF=1 m=1
XC16[104] net16 outn sky130_fd_pr__cap_mim_m3_1 W=1 L=1 MF=1 m=1
XC16[103] net16 outn sky130_fd_pr__cap_mim_m3_1 W=1 L=1 MF=1 m=1
XC16[102] net16 outn sky130_fd_pr__cap_mim_m3_1 W=1 L=1 MF=1 m=1
XC16[101] net16 outn sky130_fd_pr__cap_mim_m3_1 W=1 L=1 MF=1 m=1
XC16[100] net16 outn sky130_fd_pr__cap_mim_m3_1 W=1 L=1 MF=1 m=1
XC16[99] net16 outn sky130_fd_pr__cap_mim_m3_1 W=1 L=1 MF=1 m=1
XC16[98] net16 outn sky130_fd_pr__cap_mim_m3_1 W=1 L=1 MF=1 m=1
XC16[97] net16 outn sky130_fd_pr__cap_mim_m3_1 W=1 L=1 MF=1 m=1
XC16[96] net16 outn sky130_fd_pr__cap_mim_m3_1 W=1 L=1 MF=1 m=1
XC16[95] net16 outn sky130_fd_pr__cap_mim_m3_1 W=1 L=1 MF=1 m=1
XC16[94] net16 outn sky130_fd_pr__cap_mim_m3_1 W=1 L=1 MF=1 m=1
XC16[93] net16 outn sky130_fd_pr__cap_mim_m3_1 W=1 L=1 MF=1 m=1
XC16[92] net16 outn sky130_fd_pr__cap_mim_m3_1 W=1 L=1 MF=1 m=1
XC16[91] net16 outn sky130_fd_pr__cap_mim_m3_1 W=1 L=1 MF=1 m=1
XC16[90] net16 outn sky130_fd_pr__cap_mim_m3_1 W=1 L=1 MF=1 m=1
XC16[89] net16 outn sky130_fd_pr__cap_mim_m3_1 W=1 L=1 MF=1 m=1
XC16[88] net16 outn sky130_fd_pr__cap_mim_m3_1 W=1 L=1 MF=1 m=1
XC16[87] net16 outn sky130_fd_pr__cap_mim_m3_1 W=1 L=1 MF=1 m=1
XC16[86] net16 outn sky130_fd_pr__cap_mim_m3_1 W=1 L=1 MF=1 m=1
XC16[85] net16 outn sky130_fd_pr__cap_mim_m3_1 W=1 L=1 MF=1 m=1
XC16[84] net16 outn sky130_fd_pr__cap_mim_m3_1 W=1 L=1 MF=1 m=1
XC16[83] net16 outn sky130_fd_pr__cap_mim_m3_1 W=1 L=1 MF=1 m=1
XC16[82] net16 outn sky130_fd_pr__cap_mim_m3_1 W=1 L=1 MF=1 m=1
XC16[81] net16 outn sky130_fd_pr__cap_mim_m3_1 W=1 L=1 MF=1 m=1
XC16[80] net16 outn sky130_fd_pr__cap_mim_m3_1 W=1 L=1 MF=1 m=1
XC16[79] net16 outn sky130_fd_pr__cap_mim_m3_1 W=1 L=1 MF=1 m=1
XC16[78] net16 outn sky130_fd_pr__cap_mim_m3_1 W=1 L=1 MF=1 m=1
XC16[77] net16 outn sky130_fd_pr__cap_mim_m3_1 W=1 L=1 MF=1 m=1
XC16[76] net16 outn sky130_fd_pr__cap_mim_m3_1 W=1 L=1 MF=1 m=1
XC16[75] net16 outn sky130_fd_pr__cap_mim_m3_1 W=1 L=1 MF=1 m=1
XC16[74] net16 outn sky130_fd_pr__cap_mim_m3_1 W=1 L=1 MF=1 m=1
XC16[73] net16 outn sky130_fd_pr__cap_mim_m3_1 W=1 L=1 MF=1 m=1
XC16[72] net16 outn sky130_fd_pr__cap_mim_m3_1 W=1 L=1 MF=1 m=1
XC16[71] net16 outn sky130_fd_pr__cap_mim_m3_1 W=1 L=1 MF=1 m=1
XC16[70] net16 outn sky130_fd_pr__cap_mim_m3_1 W=1 L=1 MF=1 m=1
XC16[69] net16 outn sky130_fd_pr__cap_mim_m3_1 W=1 L=1 MF=1 m=1
XC16[68] net16 outn sky130_fd_pr__cap_mim_m3_1 W=1 L=1 MF=1 m=1
XC16[67] net16 outn sky130_fd_pr__cap_mim_m3_1 W=1 L=1 MF=1 m=1
XC16[66] net16 outn sky130_fd_pr__cap_mim_m3_1 W=1 L=1 MF=1 m=1
XC16[65] net16 outn sky130_fd_pr__cap_mim_m3_1 W=1 L=1 MF=1 m=1
XC16[64] net16 outn sky130_fd_pr__cap_mim_m3_1 W=1 L=1 MF=1 m=1
XC16[63] net16 outn sky130_fd_pr__cap_mim_m3_1 W=1 L=1 MF=1 m=1
XC16[62] net16 outn sky130_fd_pr__cap_mim_m3_1 W=1 L=1 MF=1 m=1
XC16[61] net16 outn sky130_fd_pr__cap_mim_m3_1 W=1 L=1 MF=1 m=1
XC16[60] net16 outn sky130_fd_pr__cap_mim_m3_1 W=1 L=1 MF=1 m=1
XC16[59] net16 outn sky130_fd_pr__cap_mim_m3_1 W=1 L=1 MF=1 m=1
XC16[58] net16 outn sky130_fd_pr__cap_mim_m3_1 W=1 L=1 MF=1 m=1
XC16[57] net16 outn sky130_fd_pr__cap_mim_m3_1 W=1 L=1 MF=1 m=1
XC16[56] net16 outn sky130_fd_pr__cap_mim_m3_1 W=1 L=1 MF=1 m=1
XC16[55] net16 outn sky130_fd_pr__cap_mim_m3_1 W=1 L=1 MF=1 m=1
XC16[54] net16 outn sky130_fd_pr__cap_mim_m3_1 W=1 L=1 MF=1 m=1
XC16[53] net16 outn sky130_fd_pr__cap_mim_m3_1 W=1 L=1 MF=1 m=1
XC16[52] net16 outn sky130_fd_pr__cap_mim_m3_1 W=1 L=1 MF=1 m=1
XC16[51] net16 outn sky130_fd_pr__cap_mim_m3_1 W=1 L=1 MF=1 m=1
XC16[50] net16 outn sky130_fd_pr__cap_mim_m3_1 W=1 L=1 MF=1 m=1
XC16[49] net16 outn sky130_fd_pr__cap_mim_m3_1 W=1 L=1 MF=1 m=1
XC16[48] net16 outn sky130_fd_pr__cap_mim_m3_1 W=1 L=1 MF=1 m=1
XC16[47] net16 outn sky130_fd_pr__cap_mim_m3_1 W=1 L=1 MF=1 m=1
XC16[46] net16 outn sky130_fd_pr__cap_mim_m3_1 W=1 L=1 MF=1 m=1
XC16[45] net16 outn sky130_fd_pr__cap_mim_m3_1 W=1 L=1 MF=1 m=1
XC16[44] net16 outn sky130_fd_pr__cap_mim_m3_1 W=1 L=1 MF=1 m=1
XC16[43] net16 outn sky130_fd_pr__cap_mim_m3_1 W=1 L=1 MF=1 m=1
XC16[42] net16 outn sky130_fd_pr__cap_mim_m3_1 W=1 L=1 MF=1 m=1
XC16[41] net16 outn sky130_fd_pr__cap_mim_m3_1 W=1 L=1 MF=1 m=1
XC16[40] net16 outn sky130_fd_pr__cap_mim_m3_1 W=1 L=1 MF=1 m=1
XC16[39] net16 outn sky130_fd_pr__cap_mim_m3_1 W=1 L=1 MF=1 m=1
XC16[38] net16 outn sky130_fd_pr__cap_mim_m3_1 W=1 L=1 MF=1 m=1
XC16[37] net16 outn sky130_fd_pr__cap_mim_m3_1 W=1 L=1 MF=1 m=1
XC16[36] net16 outn sky130_fd_pr__cap_mim_m3_1 W=1 L=1 MF=1 m=1
XC16[35] net16 outn sky130_fd_pr__cap_mim_m3_1 W=1 L=1 MF=1 m=1
XC16[34] net16 outn sky130_fd_pr__cap_mim_m3_1 W=1 L=1 MF=1 m=1
XC16[33] net16 outn sky130_fd_pr__cap_mim_m3_1 W=1 L=1 MF=1 m=1
XC16[32] net16 outn sky130_fd_pr__cap_mim_m3_1 W=1 L=1 MF=1 m=1
XC16[31] net16 outn sky130_fd_pr__cap_mim_m3_1 W=1 L=1 MF=1 m=1
XC16[30] net16 outn sky130_fd_pr__cap_mim_m3_1 W=1 L=1 MF=1 m=1
XC16[29] net16 outn sky130_fd_pr__cap_mim_m3_1 W=1 L=1 MF=1 m=1
XC16[28] net16 outn sky130_fd_pr__cap_mim_m3_1 W=1 L=1 MF=1 m=1
XC16[27] net16 outn sky130_fd_pr__cap_mim_m3_1 W=1 L=1 MF=1 m=1
XC16[26] net16 outn sky130_fd_pr__cap_mim_m3_1 W=1 L=1 MF=1 m=1
XC16[25] net16 outn sky130_fd_pr__cap_mim_m3_1 W=1 L=1 MF=1 m=1
XC16[24] net16 outn sky130_fd_pr__cap_mim_m3_1 W=1 L=1 MF=1 m=1
XC16[23] net16 outn sky130_fd_pr__cap_mim_m3_1 W=1 L=1 MF=1 m=1
XC16[22] net16 outn sky130_fd_pr__cap_mim_m3_1 W=1 L=1 MF=1 m=1
XC16[21] net16 outn sky130_fd_pr__cap_mim_m3_1 W=1 L=1 MF=1 m=1
XC16[20] net16 outn sky130_fd_pr__cap_mim_m3_1 W=1 L=1 MF=1 m=1
XC16[19] net16 outn sky130_fd_pr__cap_mim_m3_1 W=1 L=1 MF=1 m=1
XC16[18] net16 outn sky130_fd_pr__cap_mim_m3_1 W=1 L=1 MF=1 m=1
XC16[17] net16 outn sky130_fd_pr__cap_mim_m3_1 W=1 L=1 MF=1 m=1
XC16[16] net16 outn sky130_fd_pr__cap_mim_m3_1 W=1 L=1 MF=1 m=1
XC16[15] net16 outn sky130_fd_pr__cap_mim_m3_1 W=1 L=1 MF=1 m=1
XC16[14] net16 outn sky130_fd_pr__cap_mim_m3_1 W=1 L=1 MF=1 m=1
XC16[13] net16 outn sky130_fd_pr__cap_mim_m3_1 W=1 L=1 MF=1 m=1
XC16[12] net16 outn sky130_fd_pr__cap_mim_m3_1 W=1 L=1 MF=1 m=1
XC16[11] net16 outn sky130_fd_pr__cap_mim_m3_1 W=1 L=1 MF=1 m=1
XC16[10] net16 outn sky130_fd_pr__cap_mim_m3_1 W=1 L=1 MF=1 m=1
XC16[9] net16 outn sky130_fd_pr__cap_mim_m3_1 W=1 L=1 MF=1 m=1
XC16[8] net16 outn sky130_fd_pr__cap_mim_m3_1 W=1 L=1 MF=1 m=1
XC16[7] net16 outn sky130_fd_pr__cap_mim_m3_1 W=1 L=1 MF=1 m=1
XC16[6] net16 outn sky130_fd_pr__cap_mim_m3_1 W=1 L=1 MF=1 m=1
XC16[5] net16 outn sky130_fd_pr__cap_mim_m3_1 W=1 L=1 MF=1 m=1
XC16[4] net16 outn sky130_fd_pr__cap_mim_m3_1 W=1 L=1 MF=1 m=1
XC16[3] net16 outn sky130_fd_pr__cap_mim_m3_1 W=1 L=1 MF=1 m=1
XC16[2] net16 outn sky130_fd_pr__cap_mim_m3_1 W=1 L=1 MF=1 m=1
XC16[1] net16 outn sky130_fd_pr__cap_mim_m3_1 W=1 L=1 MF=1 m=1
XC16[0] net16 outn sky130_fd_pr__cap_mim_m3_1 W=1 L=1 MF=1 m=1
XM22[1] net15 sw[7] net16 GND sky130_fd_pr__nfet_01v8_lvt L=0.15 W=4.8 nf=11 ad='int((nf+1)/2) * W/nf * 0.29'
+ as='int((nf+2)/2) * W/nf * 0.29' pd='2*int((nf+1)/2) * (W/nf + 0.29)' ps='2*int((nf+2)/2) * (W/nf + 0.29)'
+ nrd='0.29 / W' nrs='0.29 / W' sa=0 sb=0 sd=0 mult=1 m=1
XM22[0] net15 sw[7] net16 GND sky130_fd_pr__nfet_01v8_lvt L=0.15 W=4.8 nf=11 ad='int((nf+1)/2) * W/nf * 0.29'
+ as='int((nf+2)/2) * W/nf * 0.29' pd='2*int((nf+1)/2) * (W/nf + 0.29)' ps='2*int((nf+2)/2) * (W/nf + 0.29)'
+ nrd='0.29 / W' nrs='0.29 / W' sa=0 sb=0 sd=0 mult=1 m=1
XM23 GND sw[7] net15 GND sky130_fd_pr__nfet_01v8_lvt L=0.15 W=4.8 nf=2 ad='int((nf+1)/2) * W/nf * 0.29'
+ as='int((nf+2)/2) * W/nf * 0.29' pd='2*int((nf+1)/2) * (W/nf + 0.29)' ps='2*int((nf+2)/2) * (W/nf + 0.29)'
+ nrd='0.29 / W' nrs='0.29 / W' sa=0 sb=0 sd=0 mult=1 m=1
XM24 GND sw[7] net16 GND sky130_fd_pr__nfet_01v8_lvt L=0.15 W=4.8 nf=2 ad='int((nf+1)/2) * W/nf * 0.29'
+ as='int((nf+2)/2) * W/nf * 0.29' pd='2*int((nf+1)/2) * (W/nf + 0.29)' ps='2*int((nf+2)/2) * (W/nf + 0.29)'
+ nrd='0.29 / W' nrs='0.29 / W' sa=0 sb=0 sd=0 mult=1 m=1
XC15[127] outp net15 sky130_fd_pr__cap_mim_m3_1 W=1 L=1 MF=1 m=1
XC15[126] outp net15 sky130_fd_pr__cap_mim_m3_1 W=1 L=1 MF=1 m=1
XC15[125] outp net15 sky130_fd_pr__cap_mim_m3_1 W=1 L=1 MF=1 m=1
XC15[124] outp net15 sky130_fd_pr__cap_mim_m3_1 W=1 L=1 MF=1 m=1
XC15[123] outp net15 sky130_fd_pr__cap_mim_m3_1 W=1 L=1 MF=1 m=1
XC15[122] outp net15 sky130_fd_pr__cap_mim_m3_1 W=1 L=1 MF=1 m=1
XC15[121] outp net15 sky130_fd_pr__cap_mim_m3_1 W=1 L=1 MF=1 m=1
XC15[120] outp net15 sky130_fd_pr__cap_mim_m3_1 W=1 L=1 MF=1 m=1
XC15[119] outp net15 sky130_fd_pr__cap_mim_m3_1 W=1 L=1 MF=1 m=1
XC15[118] outp net15 sky130_fd_pr__cap_mim_m3_1 W=1 L=1 MF=1 m=1
XC15[117] outp net15 sky130_fd_pr__cap_mim_m3_1 W=1 L=1 MF=1 m=1
XC15[116] outp net15 sky130_fd_pr__cap_mim_m3_1 W=1 L=1 MF=1 m=1
XC15[115] outp net15 sky130_fd_pr__cap_mim_m3_1 W=1 L=1 MF=1 m=1
XC15[114] outp net15 sky130_fd_pr__cap_mim_m3_1 W=1 L=1 MF=1 m=1
XC15[113] outp net15 sky130_fd_pr__cap_mim_m3_1 W=1 L=1 MF=1 m=1
XC15[112] outp net15 sky130_fd_pr__cap_mim_m3_1 W=1 L=1 MF=1 m=1
XC15[111] outp net15 sky130_fd_pr__cap_mim_m3_1 W=1 L=1 MF=1 m=1
XC15[110] outp net15 sky130_fd_pr__cap_mim_m3_1 W=1 L=1 MF=1 m=1
XC15[109] outp net15 sky130_fd_pr__cap_mim_m3_1 W=1 L=1 MF=1 m=1
XC15[108] outp net15 sky130_fd_pr__cap_mim_m3_1 W=1 L=1 MF=1 m=1
XC15[107] outp net15 sky130_fd_pr__cap_mim_m3_1 W=1 L=1 MF=1 m=1
XC15[106] outp net15 sky130_fd_pr__cap_mim_m3_1 W=1 L=1 MF=1 m=1
XC15[105] outp net15 sky130_fd_pr__cap_mim_m3_1 W=1 L=1 MF=1 m=1
XC15[104] outp net15 sky130_fd_pr__cap_mim_m3_1 W=1 L=1 MF=1 m=1
XC15[103] outp net15 sky130_fd_pr__cap_mim_m3_1 W=1 L=1 MF=1 m=1
XC15[102] outp net15 sky130_fd_pr__cap_mim_m3_1 W=1 L=1 MF=1 m=1
XC15[101] outp net15 sky130_fd_pr__cap_mim_m3_1 W=1 L=1 MF=1 m=1
XC15[100] outp net15 sky130_fd_pr__cap_mim_m3_1 W=1 L=1 MF=1 m=1
XC15[99] outp net15 sky130_fd_pr__cap_mim_m3_1 W=1 L=1 MF=1 m=1
XC15[98] outp net15 sky130_fd_pr__cap_mim_m3_1 W=1 L=1 MF=1 m=1
XC15[97] outp net15 sky130_fd_pr__cap_mim_m3_1 W=1 L=1 MF=1 m=1
XC15[96] outp net15 sky130_fd_pr__cap_mim_m3_1 W=1 L=1 MF=1 m=1
XC15[95] outp net15 sky130_fd_pr__cap_mim_m3_1 W=1 L=1 MF=1 m=1
XC15[94] outp net15 sky130_fd_pr__cap_mim_m3_1 W=1 L=1 MF=1 m=1
XC15[93] outp net15 sky130_fd_pr__cap_mim_m3_1 W=1 L=1 MF=1 m=1
XC15[92] outp net15 sky130_fd_pr__cap_mim_m3_1 W=1 L=1 MF=1 m=1
XC15[91] outp net15 sky130_fd_pr__cap_mim_m3_1 W=1 L=1 MF=1 m=1
XC15[90] outp net15 sky130_fd_pr__cap_mim_m3_1 W=1 L=1 MF=1 m=1
XC15[89] outp net15 sky130_fd_pr__cap_mim_m3_1 W=1 L=1 MF=1 m=1
XC15[88] outp net15 sky130_fd_pr__cap_mim_m3_1 W=1 L=1 MF=1 m=1
XC15[87] outp net15 sky130_fd_pr__cap_mim_m3_1 W=1 L=1 MF=1 m=1
XC15[86] outp net15 sky130_fd_pr__cap_mim_m3_1 W=1 L=1 MF=1 m=1
XC15[85] outp net15 sky130_fd_pr__cap_mim_m3_1 W=1 L=1 MF=1 m=1
XC15[84] outp net15 sky130_fd_pr__cap_mim_m3_1 W=1 L=1 MF=1 m=1
XC15[83] outp net15 sky130_fd_pr__cap_mim_m3_1 W=1 L=1 MF=1 m=1
XC15[82] outp net15 sky130_fd_pr__cap_mim_m3_1 W=1 L=1 MF=1 m=1
XC15[81] outp net15 sky130_fd_pr__cap_mim_m3_1 W=1 L=1 MF=1 m=1
XC15[80] outp net15 sky130_fd_pr__cap_mim_m3_1 W=1 L=1 MF=1 m=1
XC15[79] outp net15 sky130_fd_pr__cap_mim_m3_1 W=1 L=1 MF=1 m=1
XC15[78] outp net15 sky130_fd_pr__cap_mim_m3_1 W=1 L=1 MF=1 m=1
XC15[77] outp net15 sky130_fd_pr__cap_mim_m3_1 W=1 L=1 MF=1 m=1
XC15[76] outp net15 sky130_fd_pr__cap_mim_m3_1 W=1 L=1 MF=1 m=1
XC15[75] outp net15 sky130_fd_pr__cap_mim_m3_1 W=1 L=1 MF=1 m=1
XC15[74] outp net15 sky130_fd_pr__cap_mim_m3_1 W=1 L=1 MF=1 m=1
XC15[73] outp net15 sky130_fd_pr__cap_mim_m3_1 W=1 L=1 MF=1 m=1
XC15[72] outp net15 sky130_fd_pr__cap_mim_m3_1 W=1 L=1 MF=1 m=1
XC15[71] outp net15 sky130_fd_pr__cap_mim_m3_1 W=1 L=1 MF=1 m=1
XC15[70] outp net15 sky130_fd_pr__cap_mim_m3_1 W=1 L=1 MF=1 m=1
XC15[69] outp net15 sky130_fd_pr__cap_mim_m3_1 W=1 L=1 MF=1 m=1
XC15[68] outp net15 sky130_fd_pr__cap_mim_m3_1 W=1 L=1 MF=1 m=1
XC15[67] outp net15 sky130_fd_pr__cap_mim_m3_1 W=1 L=1 MF=1 m=1
XC15[66] outp net15 sky130_fd_pr__cap_mim_m3_1 W=1 L=1 MF=1 m=1
XC15[65] outp net15 sky130_fd_pr__cap_mim_m3_1 W=1 L=1 MF=1 m=1
XC15[64] outp net15 sky130_fd_pr__cap_mim_m3_1 W=1 L=1 MF=1 m=1
XC15[63] outp net15 sky130_fd_pr__cap_mim_m3_1 W=1 L=1 MF=1 m=1
XC15[62] outp net15 sky130_fd_pr__cap_mim_m3_1 W=1 L=1 MF=1 m=1
XC15[61] outp net15 sky130_fd_pr__cap_mim_m3_1 W=1 L=1 MF=1 m=1
XC15[60] outp net15 sky130_fd_pr__cap_mim_m3_1 W=1 L=1 MF=1 m=1
XC15[59] outp net15 sky130_fd_pr__cap_mim_m3_1 W=1 L=1 MF=1 m=1
XC15[58] outp net15 sky130_fd_pr__cap_mim_m3_1 W=1 L=1 MF=1 m=1
XC15[57] outp net15 sky130_fd_pr__cap_mim_m3_1 W=1 L=1 MF=1 m=1
XC15[56] outp net15 sky130_fd_pr__cap_mim_m3_1 W=1 L=1 MF=1 m=1
XC15[55] outp net15 sky130_fd_pr__cap_mim_m3_1 W=1 L=1 MF=1 m=1
XC15[54] outp net15 sky130_fd_pr__cap_mim_m3_1 W=1 L=1 MF=1 m=1
XC15[53] outp net15 sky130_fd_pr__cap_mim_m3_1 W=1 L=1 MF=1 m=1
XC15[52] outp net15 sky130_fd_pr__cap_mim_m3_1 W=1 L=1 MF=1 m=1
XC15[51] outp net15 sky130_fd_pr__cap_mim_m3_1 W=1 L=1 MF=1 m=1
XC15[50] outp net15 sky130_fd_pr__cap_mim_m3_1 W=1 L=1 MF=1 m=1
XC15[49] outp net15 sky130_fd_pr__cap_mim_m3_1 W=1 L=1 MF=1 m=1
XC15[48] outp net15 sky130_fd_pr__cap_mim_m3_1 W=1 L=1 MF=1 m=1
XC15[47] outp net15 sky130_fd_pr__cap_mim_m3_1 W=1 L=1 MF=1 m=1
XC15[46] outp net15 sky130_fd_pr__cap_mim_m3_1 W=1 L=1 MF=1 m=1
XC15[45] outp net15 sky130_fd_pr__cap_mim_m3_1 W=1 L=1 MF=1 m=1
XC15[44] outp net15 sky130_fd_pr__cap_mim_m3_1 W=1 L=1 MF=1 m=1
XC15[43] outp net15 sky130_fd_pr__cap_mim_m3_1 W=1 L=1 MF=1 m=1
XC15[42] outp net15 sky130_fd_pr__cap_mim_m3_1 W=1 L=1 MF=1 m=1
XC15[41] outp net15 sky130_fd_pr__cap_mim_m3_1 W=1 L=1 MF=1 m=1
XC15[40] outp net15 sky130_fd_pr__cap_mim_m3_1 W=1 L=1 MF=1 m=1
XC15[39] outp net15 sky130_fd_pr__cap_mim_m3_1 W=1 L=1 MF=1 m=1
XC15[38] outp net15 sky130_fd_pr__cap_mim_m3_1 W=1 L=1 MF=1 m=1
XC15[37] outp net15 sky130_fd_pr__cap_mim_m3_1 W=1 L=1 MF=1 m=1
XC15[36] outp net15 sky130_fd_pr__cap_mim_m3_1 W=1 L=1 MF=1 m=1
XC15[35] outp net15 sky130_fd_pr__cap_mim_m3_1 W=1 L=1 MF=1 m=1
XC15[34] outp net15 sky130_fd_pr__cap_mim_m3_1 W=1 L=1 MF=1 m=1
XC15[33] outp net15 sky130_fd_pr__cap_mim_m3_1 W=1 L=1 MF=1 m=1
XC15[32] outp net15 sky130_fd_pr__cap_mim_m3_1 W=1 L=1 MF=1 m=1
XC15[31] outp net15 sky130_fd_pr__cap_mim_m3_1 W=1 L=1 MF=1 m=1
XC15[30] outp net15 sky130_fd_pr__cap_mim_m3_1 W=1 L=1 MF=1 m=1
XC15[29] outp net15 sky130_fd_pr__cap_mim_m3_1 W=1 L=1 MF=1 m=1
XC15[28] outp net15 sky130_fd_pr__cap_mim_m3_1 W=1 L=1 MF=1 m=1
XC15[27] outp net15 sky130_fd_pr__cap_mim_m3_1 W=1 L=1 MF=1 m=1
XC15[26] outp net15 sky130_fd_pr__cap_mim_m3_1 W=1 L=1 MF=1 m=1
XC15[25] outp net15 sky130_fd_pr__cap_mim_m3_1 W=1 L=1 MF=1 m=1
XC15[24] outp net15 sky130_fd_pr__cap_mim_m3_1 W=1 L=1 MF=1 m=1
XC15[23] outp net15 sky130_fd_pr__cap_mim_m3_1 W=1 L=1 MF=1 m=1
XC15[22] outp net15 sky130_fd_pr__cap_mim_m3_1 W=1 L=1 MF=1 m=1
XC15[21] outp net15 sky130_fd_pr__cap_mim_m3_1 W=1 L=1 MF=1 m=1
XC15[20] outp net15 sky130_fd_pr__cap_mim_m3_1 W=1 L=1 MF=1 m=1
XC15[19] outp net15 sky130_fd_pr__cap_mim_m3_1 W=1 L=1 MF=1 m=1
XC15[18] outp net15 sky130_fd_pr__cap_mim_m3_1 W=1 L=1 MF=1 m=1
XC15[17] outp net15 sky130_fd_pr__cap_mim_m3_1 W=1 L=1 MF=1 m=1
XC15[16] outp net15 sky130_fd_pr__cap_mim_m3_1 W=1 L=1 MF=1 m=1
XC15[15] outp net15 sky130_fd_pr__cap_mim_m3_1 W=1 L=1 MF=1 m=1
XC15[14] outp net15 sky130_fd_pr__cap_mim_m3_1 W=1 L=1 MF=1 m=1
XC15[13] outp net15 sky130_fd_pr__cap_mim_m3_1 W=1 L=1 MF=1 m=1
XC15[12] outp net15 sky130_fd_pr__cap_mim_m3_1 W=1 L=1 MF=1 m=1
XC15[11] outp net15 sky130_fd_pr__cap_mim_m3_1 W=1 L=1 MF=1 m=1
XC15[10] outp net15 sky130_fd_pr__cap_mim_m3_1 W=1 L=1 MF=1 m=1
XC15[9] outp net15 sky130_fd_pr__cap_mim_m3_1 W=1 L=1 MF=1 m=1
XC15[8] outp net15 sky130_fd_pr__cap_mim_m3_1 W=1 L=1 MF=1 m=1
XC15[7] outp net15 sky130_fd_pr__cap_mim_m3_1 W=1 L=1 MF=1 m=1
XC15[6] outp net15 sky130_fd_pr__cap_mim_m3_1 W=1 L=1 MF=1 m=1
XC15[5] outp net15 sky130_fd_pr__cap_mim_m3_1 W=1 L=1 MF=1 m=1
XC15[4] outp net15 sky130_fd_pr__cap_mim_m3_1 W=1 L=1 MF=1 m=1
XC15[3] outp net15 sky130_fd_pr__cap_mim_m3_1 W=1 L=1 MF=1 m=1
XC15[2] outp net15 sky130_fd_pr__cap_mim_m3_1 W=1 L=1 MF=1 m=1
XC15[1] outp net15 sky130_fd_pr__cap_mim_m3_1 W=1 L=1 MF=1 m=1
XC15[0] outp net15 sky130_fd_pr__cap_mim_m3_1 W=1 L=1 MF=1 m=1
**.ends
.GLOBAL GND
.end
